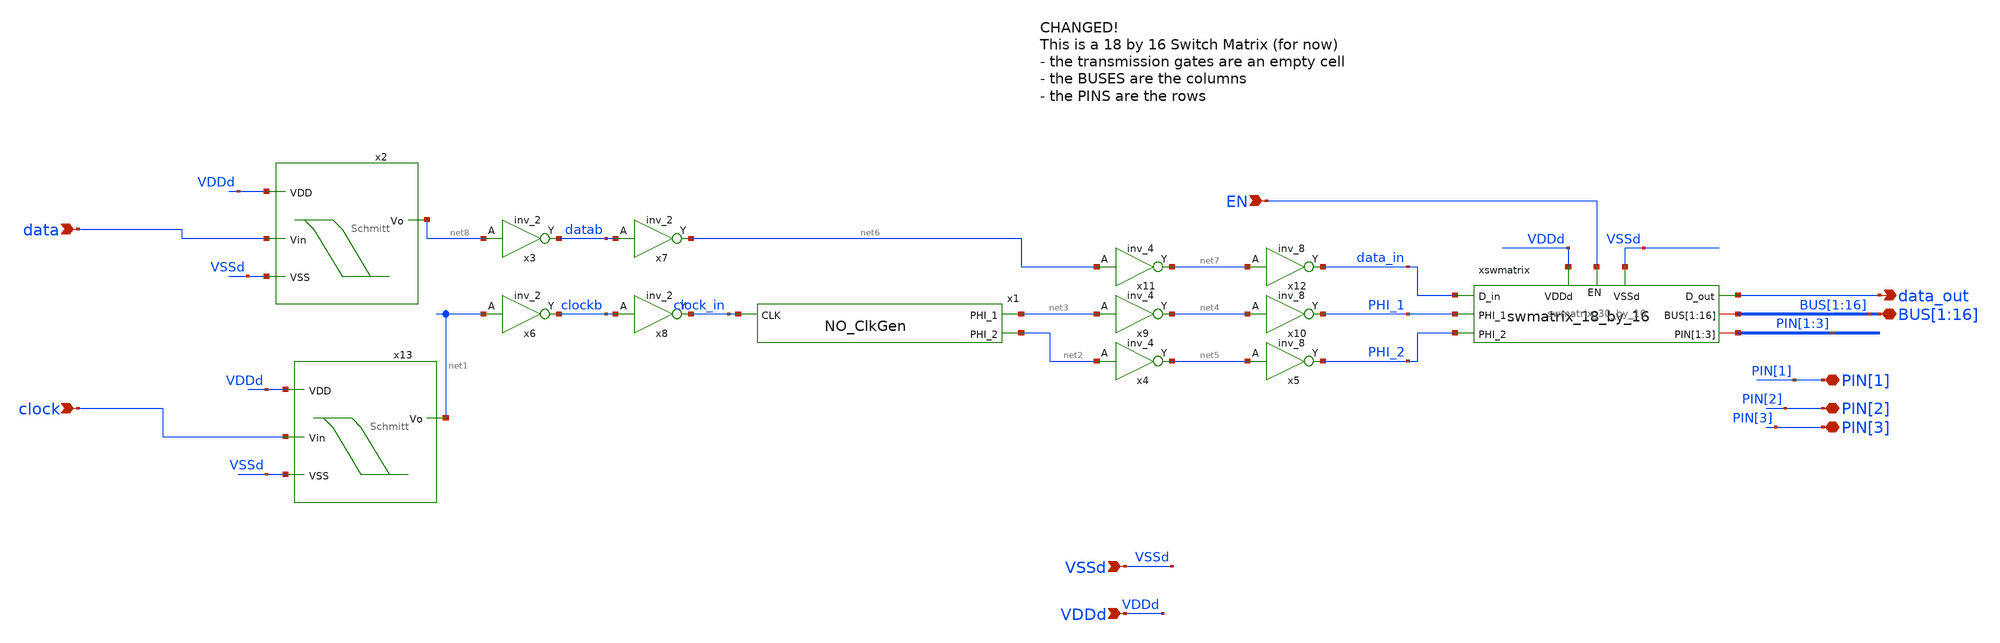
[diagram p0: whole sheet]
** sch_path: designs/Swmatrix.sch
**.subckt Swmatrix data clock EN VDDd VSSd data_out
*+ BUS[1],BUS[2],BUS[3],BUS[4],BUS[5],BUS[6],BUS[7],BUS[8],BUS[9],BUS[10],BUS[11],BUS[12],BUS[13],BUS[14],BUS[15],BUS[16] PIN[1] PIN[3] PIN[2]
*.ipin data
*.ipin clock
*.ipin EN
*.ipin VDDd
*.ipin VSSd
*.opin data_out
*.iopin
*+ BUS[1],BUS[2],BUS[3],BUS[4],BUS[5],BUS[6],BUS[7],BUS[8],BUS[9],BUS[10],BUS[11],BUS[12],BUS[13],BUS[14],BUS[15],BUS[16]
*.iopin PIN[1]
*.iopin PIN[3]
*.iopin PIN[2]
x1 net2 clock_in net3 NO_ClkGen
xswmatrix data_in data_out PHI_1 PHI_2 BUS[1] BUS[2] BUS[3] BUS[4] BUS[5] BUS[6] BUS[7] BUS[8]
+ BUS[9] BUS[10] BUS[11] BUS[12] BUS[13] BUS[14] BUS[15] BUS[16] PIN[1] PIN[2] PIN[3] VSSd VDDd EN
+ swmatrix_30_by_10
x3 net8 VSSd VDDd VSSd VDDd datab gf180mcu_fd_sc_mcu9t5v0__inv_2
x4 net2 VSSd VDDd VSSd VDDd net5 gf180mcu_fd_sc_mcu9t5v0__inv_4
x5 net5 VSSd VDDd VSSd VDDd PHI_2 gf180mcu_fd_sc_mcu9t5v0__inv_8
x6 net1 VSSd VDDd VSSd VDDd clockb gf180mcu_fd_sc_mcu9t5v0__inv_2
x7 datab VSSd VDDd VSSd VDDd net6 gf180mcu_fd_sc_mcu9t5v0__inv_2
x8 clockb VSSd VDDd VSSd VDDd clock_in gf180mcu_fd_sc_mcu9t5v0__inv_2
x9 net3 VSSd VDDd VSSd VDDd net4 gf180mcu_fd_sc_mcu9t5v0__inv_4
x10 net4 VSSd VDDd VSSd VDDd PHI_1 gf180mcu_fd_sc_mcu9t5v0__inv_8
x11 net6 VSSd VDDd VSSd VDDd net7 gf180mcu_fd_sc_mcu9t5v0__inv_4
x12 net7 VSSd VDDd VSSd VDDd data_in gf180mcu_fd_sc_mcu9t5v0__inv_8
x2 VDDd data net8 VSSd Schmitt
x13 VDDd clock net1 VSSd Schmitt
**.ends
.end
